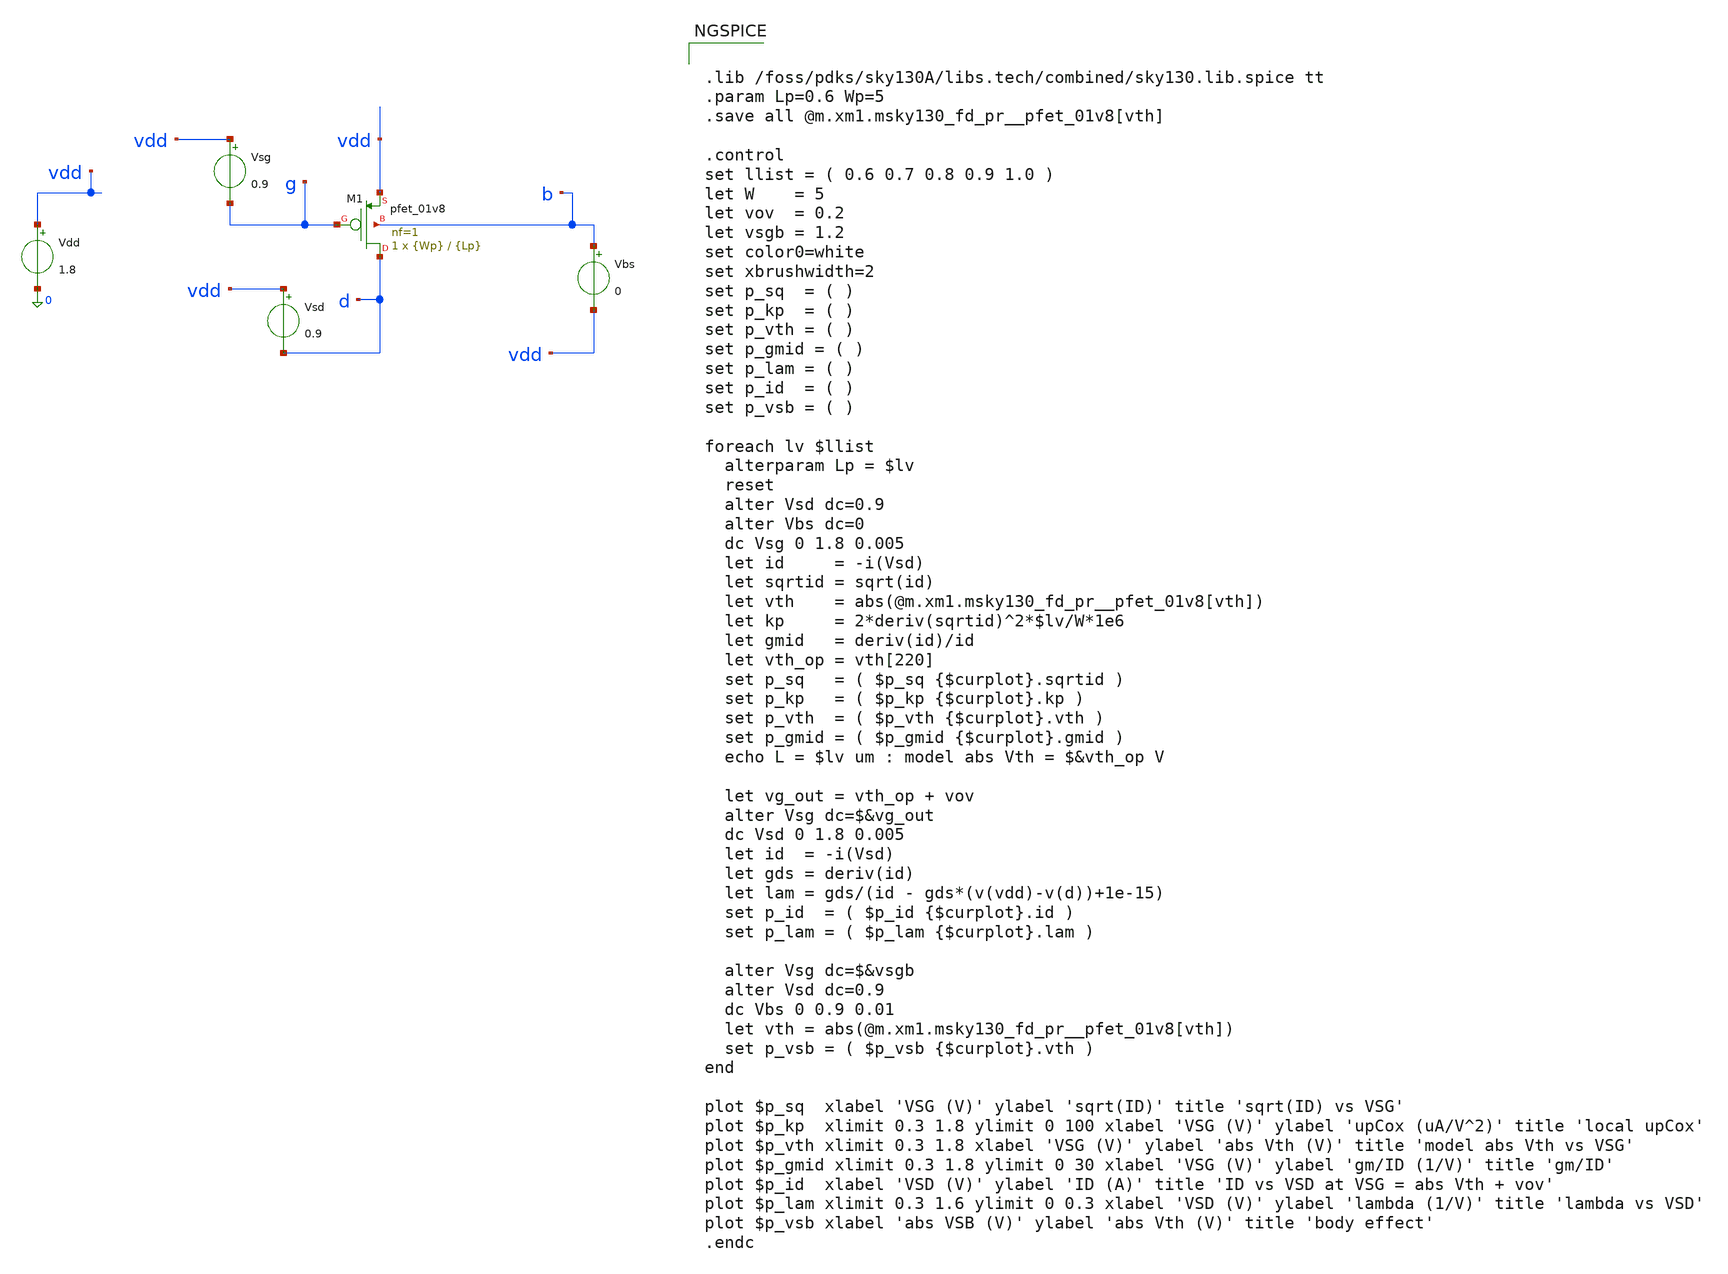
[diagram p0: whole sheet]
** sch_path: parameter_extraction/pmos_characterization.sch
**.subckt pmos_characterization
Vsg vdd g 0.9
Vbs b vdd 0
XM1 d g vdd b sky130_fd_pr__pfet_01v8 L={Lp} W={Wp} nf=1 ad='int((1 + 1)/2) * {Wp} / 1 * 0.29' as='int((1 + 2)/2) * {Wp} / 1 * 0.29'
+ pd='2*int((1 + 1)/2) * ({Wp} / 1 + 0.29)' ps='2*int((1 + 2)/2) * ({Wp} / 1 + 0.29)' nrd='0.29 / {Wp} '
+ nrs='0.29 / {Wp} ' sa=0 sb=0 sd=0 mult=1 m=1
Vdd vdd 0 1.8
Vsd vdd d 0.9
**** begin user architecture code


.lib /foss/pdks/sky130A/libs.tech/combined/sky130.lib.spice tt
.param Lp=0.6 Wp=5
.save all @m.xm1.msky130_fd_pr__pfet_01v8[vth]

.control
set llist = ( 0.6 0.7 0.8 0.9 1.0 )
let W    = 5
let vov  = 0.2
let vsgb = 1.2
set color0=white
set xbrushwidth=2
set p_sq  = ( )
set p_kp  = ( )
set p_vth = ( )
set p_gmid = ( )
set p_lam = ( )
set p_id  = ( )
set p_vsb = ( )

foreach lv $llist
  alterparam Lp = $lv
  reset
  alter Vsd dc=0.9
  alter Vbs dc=0
  dc Vsg 0 1.8 0.005
  let id     = -i(Vsd)
  let sqrtid = sqrt(id)
  let vth    = abs(@m.xm1.msky130_fd_pr__pfet_01v8[vth])
  let kp     = 2*deriv(sqrtid)^2*$lv/W*1e6
  let gmid   = deriv(id)/id
  let vth_op = vth[220]
  set p_sq   = ( $p_sq {$curplot}.sqrtid )
  set p_kp   = ( $p_kp {$curplot}.kp )
  set p_vth  = ( $p_vth {$curplot}.vth )
  set p_gmid = ( $p_gmid {$curplot}.gmid )
  echo L = $lv um : model abs Vth = $&vth_op V

  let vg_out = vth_op + vov
  alter Vsg dc=$&vg_out
  dc Vsd 0 1.8 0.005
  let id  = -i(Vsd)
  let gds = deriv(id)
  let lam = gds/(id - gds*(v(vdd)-v(d))+1e-15)
  set p_id  = ( $p_id {$curplot}.id )
  set p_lam = ( $p_lam {$curplot}.lam )

  alter Vsg dc=$&vsgb
  alter Vsd dc=0.9
  dc Vbs 0 0.9 0.01
  let vth = abs(@m.xm1.msky130_fd_pr__pfet_01v8[vth])
  set p_vsb = ( $p_vsb {$curplot}.vth )
end

plot $p_sq  xlabel 'VSG (V)' ylabel 'sqrt(ID)' title 'sqrt(ID) vs VSG'
plot $p_kp  xlimit 0.3 1.8 ylimit 0 100 xlabel 'VSG (V)' ylabel 'upCox (uA/V^2)' title 'local upCox'
plot $p_vth xlimit 0.3 1.8 xlabel 'VSG (V)' ylabel 'abs Vth (V)' title 'model abs Vth vs VSG'
plot $p_gmid xlimit 0.3 1.8 ylimit 0 30 xlabel 'VSG (V)' ylabel 'gm/ID (1/V)' title 'gm/ID'
plot $p_id  xlabel 'VSD (V)' ylabel 'ID (A)' title 'ID vs VSD at VSG = abs Vth + vov'
plot $p_lam xlimit 0.3 1.6 ylimit 0 0.3 xlabel 'VSD (V)' ylabel 'lambda (1/V)' title 'lambda vs VSD'
plot $p_vsb xlabel 'abs VSB (V)' ylabel 'abs Vth (V)' title 'body effect'
.endc


**** end user architecture code
**.ends
.end
